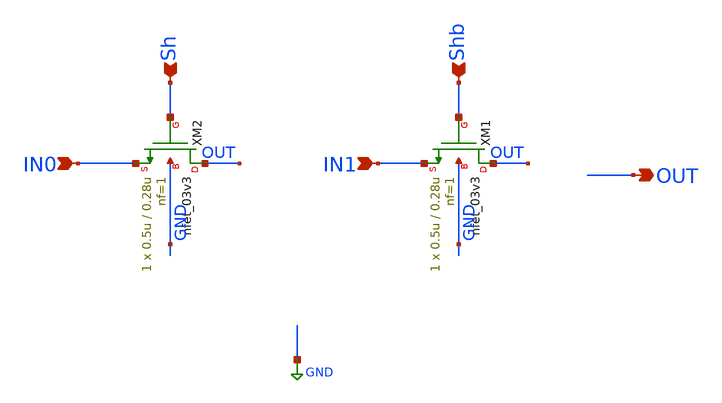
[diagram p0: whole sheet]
** sch_path: 1BIT.sch
**.subckt 1BIT Sh Shb OUT IN1 IN0
*.ipin Sh
*.ipin Shb
*.opin OUT
*.ipin IN1
*.ipin IN0
XM2 OUT Sh IN0 GND nfet_03v3 L=0.28u W=0.5u nf=1 ad='int((nf+1)/2) * W/nf * 0.18u' as='int((nf+2)/2) * W/nf * 0.18u'
+ pd='2*int((nf+1)/2) * (W/nf + 0.18u)' ps='2*int((nf+2)/2) * (W/nf + 0.18u)' nrd='0.18u / W' nrs='0.18u / W'
+ sa=0 sb=0 sd=0 m=1
XM1 OUT Shb IN1 GND nfet_03v3 L=0.28u W=0.5u nf=1 ad='int((nf+1)/2) * W/nf * 0.18u' as='int((nf+2)/2) * W/nf * 0.18u'
+ pd='2*int((nf+1)/2) * (W/nf + 0.18u)' ps='2*int((nf+2)/2) * (W/nf + 0.18u)' nrd='0.18u / W' nrs='0.18u / W'
+ sa=0 sb=0 sd=0 m=1
**.ends
.GLOBAL GND
.end
